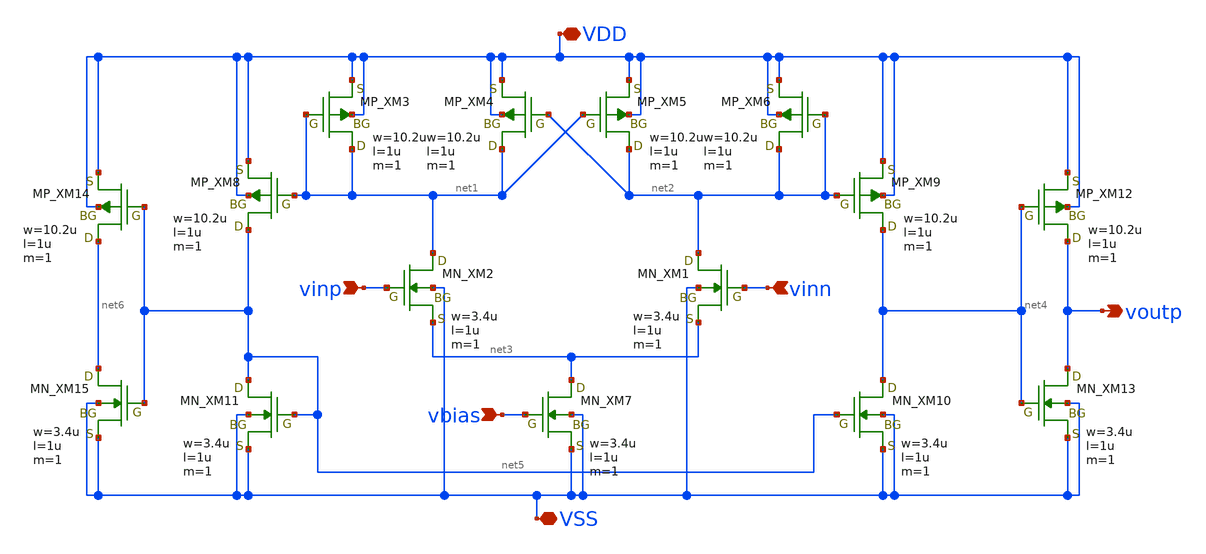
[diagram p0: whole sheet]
** sch_path: Vol.2/files/04/xschem/StrongArmcmp.sch
**.subckt StrongArmcmp VDD VSS vinp vinn vbias voutp
*.iopin VDD
*.iopin VSS
*.ipin vinp
*.ipin vinn
*.ipin vbias
*.opin voutp
XM1 net2 vinn net3 VSS NMOS w=3.4u l=1u as=0 ad=0 ps=0 pd=0 nrd=0 nrs=0 m=1
XM2 net1 vinp net3 VSS NMOS w=3.4u l=1u as=0 ad=0 ps=0 pd=0 nrd=0 nrs=0 m=1
XM3 net1 net1 VDD VDD PMOS w=10.2u l=1u as=0 ad=0 ps=0 pd=0 nrd=0 nrs=0 m=1
XM4 net1 net2 VDD VDD PMOS w=10.2u l=1u as=0 ad=0 ps=0 pd=0 nrd=0 nrs=0 m=1
XM5 net2 net1 VDD VDD PMOS w=10.2u l=1u as=0 ad=0 ps=0 pd=0 nrd=0 nrs=0 m=1
XM6 net2 net2 VDD VDD PMOS w=10.2u l=1u as=0 ad=0 ps=0 pd=0 nrd=0 nrs=0 m=1
XM7 net3 vbias VSS VSS NMOS w=3.4u l=1u as=0 ad=0 ps=0 pd=0 nrd=0 nrs=0 m=1
XM8 net5 net1 VDD VDD PMOS w=10.2u l=1u as=0 ad=0 ps=0 pd=0 nrd=0 nrs=0 m=1
XM9 net4 net2 VDD VDD PMOS w=10.2u l=1u as=0 ad=0 ps=0 pd=0 nrd=0 nrs=0 m=1
XM10 net4 net5 VSS VSS NMOS w=3.4u l=1u as=0 ad=0 ps=0 pd=0 nrd=0 nrs=0 m=1
XM11 net5 net5 VSS VSS NMOS w=3.4u l=1u as=0 ad=0 ps=0 pd=0 nrd=0 nrs=0 m=1
XM12 voutp net4 VDD VDD PMOS w=10.2u l=1u as=0 ad=0 ps=0 pd=0 nrd=0 nrs=0 m=1
XM13 voutp net4 VSS VSS NMOS w=3.4u l=1u as=0 ad=0 ps=0 pd=0 nrd=0 nrs=0 m=1
XM14 net6 net5 VDD VDD PMOS w=10.2u l=1u as=0 ad=0 ps=0 pd=0 nrd=0 nrs=0 m=1
XM15 net6 net5 VSS VSS NMOS w=3.4u l=1u as=0 ad=0 ps=0 pd=0 nrd=0 nrs=0 m=1
**.ends
.end
